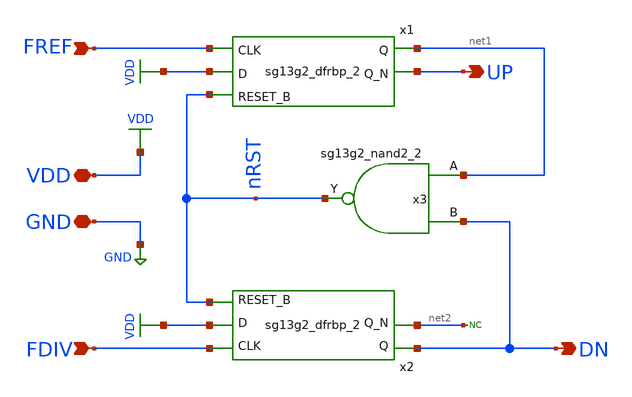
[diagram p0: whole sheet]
** sch_path: xschem/phase-freq-detector/PHASE_FREQ_DET.sch
**.subckt PHASE_FREQ_DET UP FREF VDD GND DN FDIV
*.opin UP
*.ipin FREF
*.iopin VDD
*.iopin GND
*.opin DN
*.ipin FDIV
x1 net1 UP FREF VDD nRST VDD GND sg13g2_dfrbp_2
x2 DN net2 FDIV VDD nRST VDD GND sg13g2_dfrbp_2
x3 nRST net1 DN VDD GND sg13g2_nand2_2
* noconn #net2
**.ends
.GLOBAL VDD
.GLOBAL GND
.end
